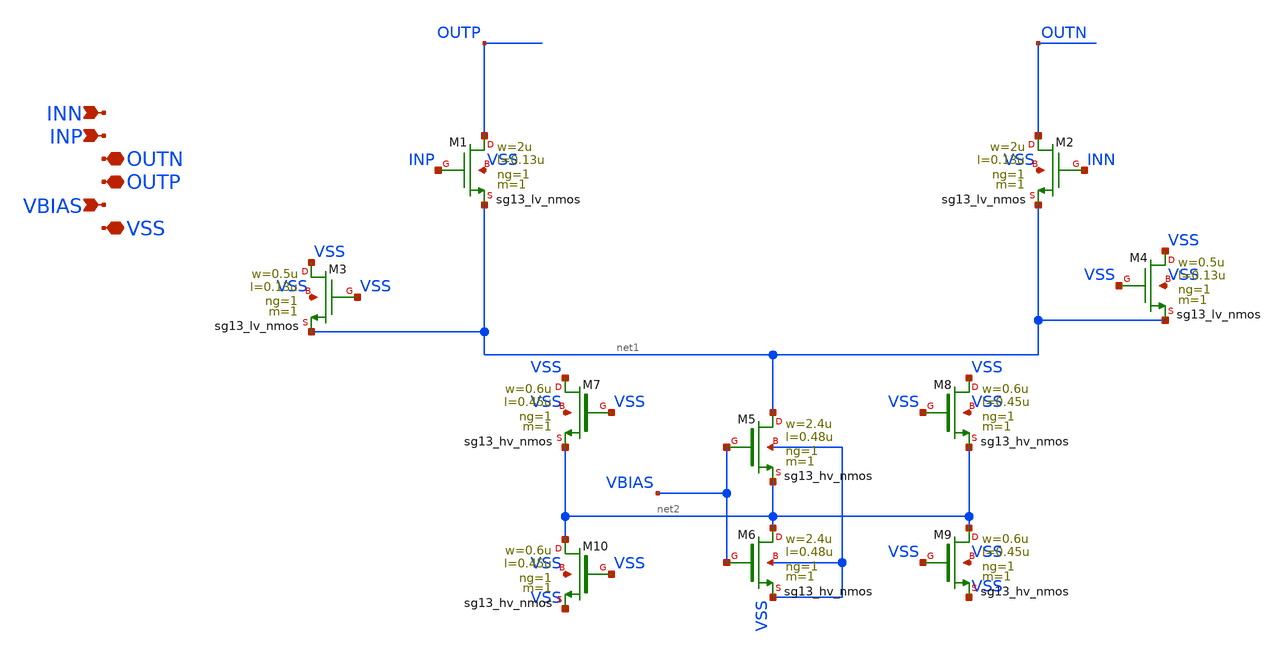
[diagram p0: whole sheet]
** sch_path: dependencies/DAC/dependencies/CS_DAC-/xschem/CS_Switch_8x.sch
**.subckt CS_Switch_8x VSS VBIAS OUTP OUTN INP INN
*.iopin VSS
*.ipin VBIAS
*.iopin OUTP
*.iopin OUTN
*.ipin INP
*.ipin INN
XM1 OUTP INP net1 VSS sg13_lv_nmos w=2u l=0.13u ng=1 m=1 mm_ok=1
XM2 OUTN INN net1 VSS sg13_lv_nmos w=2u l=0.13u ng=1 m=1 mm_ok=1
XM3 VSS VSS net1 VSS sg13_lv_nmos w=0.5u l=0.13u ng=1 m=1 mm_ok=1
XM4 VSS VSS net1 VSS sg13_lv_nmos w=0.5u l=0.13u ng=1 m=1 mm_ok=1
XM5 net1 VBIAS net2 VSS sg13_hv_nmos w=2.4u l=0.48u ng=1 m=1 mm_ok=1
XM6 net2 VBIAS VSS VSS sg13_hv_nmos w=2.4u l=0.48u ng=1 m=1 mm_ok=1
XM7 VSS VSS net2 VSS sg13_hv_nmos w=0.6u l=0.45u ng=1 m=1 mm_ok=1
XM8 VSS VSS net2 VSS sg13_hv_nmos w=0.6u l=0.45u ng=1 m=1 mm_ok=1
XM9 net2 VSS VSS VSS sg13_hv_nmos w=0.6u l=0.45u ng=1 m=1 mm_ok=1
XM10 net2 VSS VSS VSS sg13_hv_nmos w=0.6u l=0.45u ng=1 m=1 mm_ok=1
**.ends
.end
